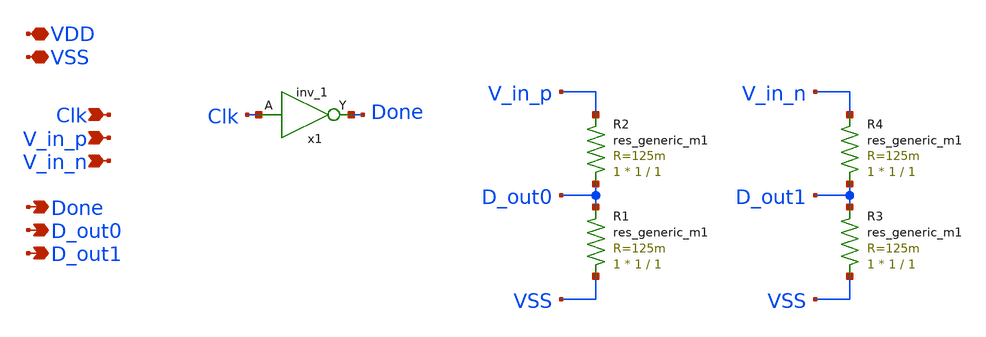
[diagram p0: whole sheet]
** sch_path: xschem/src/sar-adc/sar-adc.sch
**.subckt sar-adc VDD V_in_p Done VSS V_in_n Clk D_out0 D_out1
*.iopin VDD
*.ipin V_in_p
*.opin Done
*.iopin VSS
*.ipin V_in_n
*.ipin Clk
*.opin D_out0
*.opin D_out1
x1 Clk VSS VSS VDD VDD Done sky130_fd_sc_hd__inv_1
R1 VSS D_out0 sky130_fd_pr__res_generic_m1 W=1 L=1 m=1
R2 D_out0 V_in_p sky130_fd_pr__res_generic_m1 W=1 L=1 m=1
R3 VSS D_out1 sky130_fd_pr__res_generic_m1 W=1 L=1 m=1
R4 D_out1 V_in_n sky130_fd_pr__res_generic_m1 W=1 L=1 m=1
**** begin user architecture code
 .include $::SKYWATER_STDCELLS/sky130_fd_sc_hd.spice

**** end user architecture code
**.ends
.end
